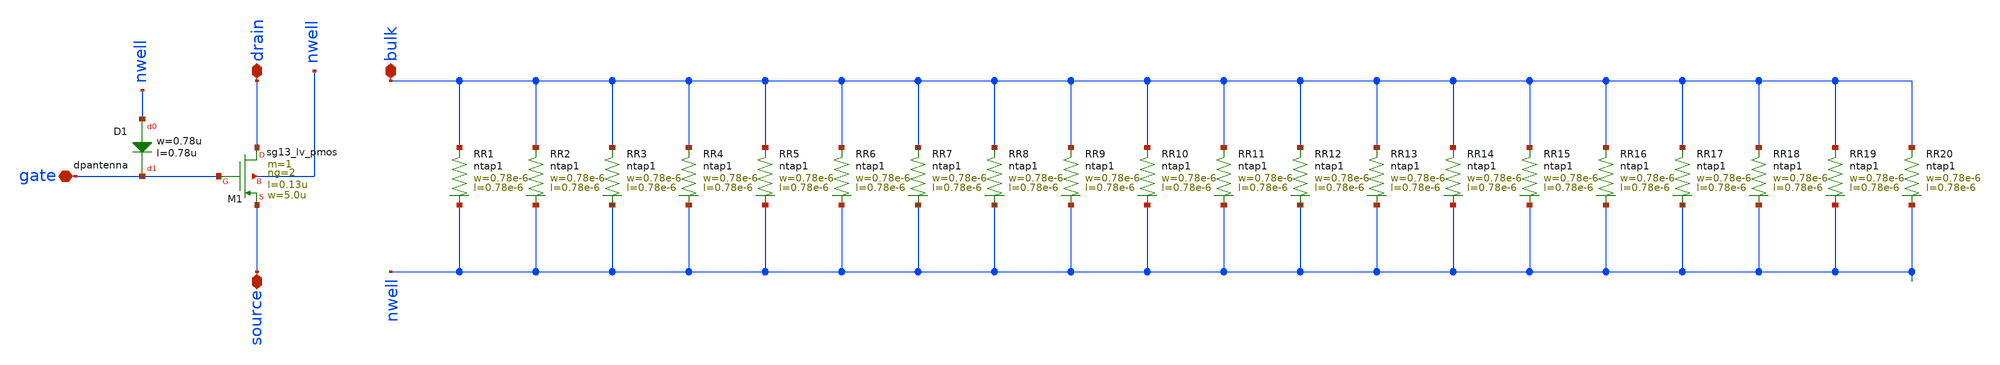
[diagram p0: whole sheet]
** sch_path: ts_pr_May2024/design_data/xschem/pmos2.sch
**.subckt pmos2 gate drain source bulk
*.iopin gate
*.iopin drain
*.iopin source
*.iopin bulk
XD1 nwell gate dpantenna l=0.78u w=0.78u
XM1 drain gate source nwell sg13_lv_pmos w=5.0u l=0.13u ng=2 m=1 mm_ok=1
XR1 bulk nwell ntap1 R=262.8 w=0.78e-6 l=0.78e-6
XR2 bulk nwell ntap1 R=262.8 w=0.78e-6 l=0.78e-6
XR3 bulk nwell ntap1 R=262.8 w=0.78e-6 l=0.78e-6
XR4 bulk nwell ntap1 R=262.8 w=0.78e-6 l=0.78e-6
XR5 bulk nwell ntap1 R=262.8 w=0.78e-6 l=0.78e-6
XR6 bulk nwell ntap1 R=262.8 w=0.78e-6 l=0.78e-6
XR7 bulk nwell ntap1 R=262.8 w=0.78e-6 l=0.78e-6
XR8 bulk nwell ntap1 R=262.8 w=0.78e-6 l=0.78e-6
XR9 bulk nwell ntap1 R=262.8 w=0.78e-6 l=0.78e-6
XR10 bulk nwell ntap1 R=262.8 w=0.78e-6 l=0.78e-6
XR11 bulk nwell ntap1 R=262.8 w=0.78e-6 l=0.78e-6
XR12 bulk nwell ntap1 R=262.8 w=0.78e-6 l=0.78e-6
XR13 bulk nwell ntap1 R=262.8 w=0.78e-6 l=0.78e-6
XR14 bulk nwell ntap1 R=262.8 w=0.78e-6 l=0.78e-6
XR15 bulk nwell ntap1 R=262.8 w=0.78e-6 l=0.78e-6
XR16 bulk nwell ntap1 R=262.8 w=0.78e-6 l=0.78e-6
XR17 bulk nwell ntap1 R=262.8 w=0.78e-6 l=0.78e-6
XR18 bulk nwell ntap1 R=262.8 w=0.78e-6 l=0.78e-6
XR19 bulk nwell ntap1 R=262.8 w=0.78e-6 l=0.78e-6
XR20 bulk nwell ntap1 R=262.8 w=0.78e-6 l=0.78e-6
**.ends
.end
